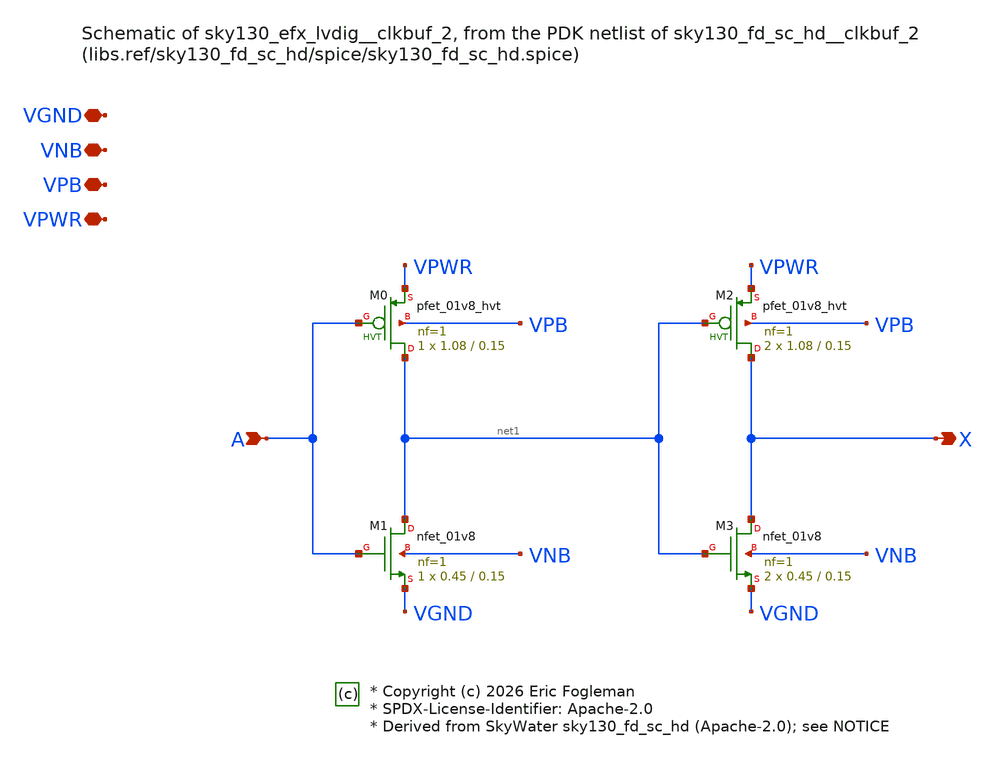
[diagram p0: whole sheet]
** sch_path: xschem/sky130_efx_lvdig__clkbuf_2.sch

* Copyright (c) 2026 Eric Fogleman
* SPDX-License-Identifier: Apache-2.0
* Derived from SkyWater sky130_fd_sc_hd (Apache-2.0); see NOTICE

**.subckt sky130_efx_lvdig__clkbuf_2 A X VGND VNB VPB VPWR
*.ipin A
*.opin X
*.iopin VGND
*.iopin VNB
*.iopin VPB
*.iopin VPWR
XM0 net1 A VPWR VPB sky130_fd_pr__pfet_01v8_hvt L=0.15 W=1.08 nf=1 ad='int((1 + 1)/2) * 1.08 / 1 * 0.29'
+ as='int((1 + 2)/2) * 1.08 / 1 * 0.29' pd='2*int((1 + 1)/2) * (1.08 / 1 + 0.29)' ps='2*int((1 + 2)/2) * (1.08 / 1 + 0.29)'
+ nrd='0.29 / 1.08 ' nrs='0.29 / 1.08 ' sa=0 sb=0 sd=0 mult=1 m=1
XM1 net1 A VGND VNB sky130_fd_pr__nfet_01v8 L=0.15 W=0.45 nf=1 ad='int((1 + 1)/2) * 0.45 / 1 * 0.29'
+ as='int((1 + 2)/2) * 0.45 / 1 * 0.29' pd='2*int((1 + 1)/2) * (0.45 / 1 + 0.29)' ps='2*int((1 + 2)/2) * (0.45 / 1 + 0.29)'
+ nrd='0.29 / 0.45 ' nrs='0.29 / 0.45 ' sa=0 sb=0 sd=0 mult=1 m=1
XM2 X net1 VPWR VPB sky130_fd_pr__pfet_01v8_hvt L=0.15 W=1.08 nf=1 ad='int((1 + 1)/2) * 1.08 / 1 * 0.29'
+ as='int((1 + 2)/2) * 1.08 / 1 * 0.29' pd='2*int((1 + 1)/2) * (1.08 / 1 + 0.29)' ps='2*int((1 + 2)/2) * (1.08 / 1 + 0.29)'
+ nrd='0.29 / 1.08 ' nrs='0.29 / 1.08 ' sa=0 sb=0 sd=0 mult=2 m=2
XM3 X net1 VGND VNB sky130_fd_pr__nfet_01v8 L=0.15 W=0.45 nf=1 ad='int((1 + 1)/2) * 0.45 / 1 * 0.29'
+ as='int((1 + 2)/2) * 0.45 / 1 * 0.29' pd='2*int((1 + 1)/2) * (0.45 / 1 + 0.29)' ps='2*int((1 + 2)/2) * (0.45 / 1 + 0.29)'
+ nrd='0.29 / 0.45 ' nrs='0.29 / 0.45 ' sa=0 sb=0 sd=0 mult=2 m=2
**.ends
.end
